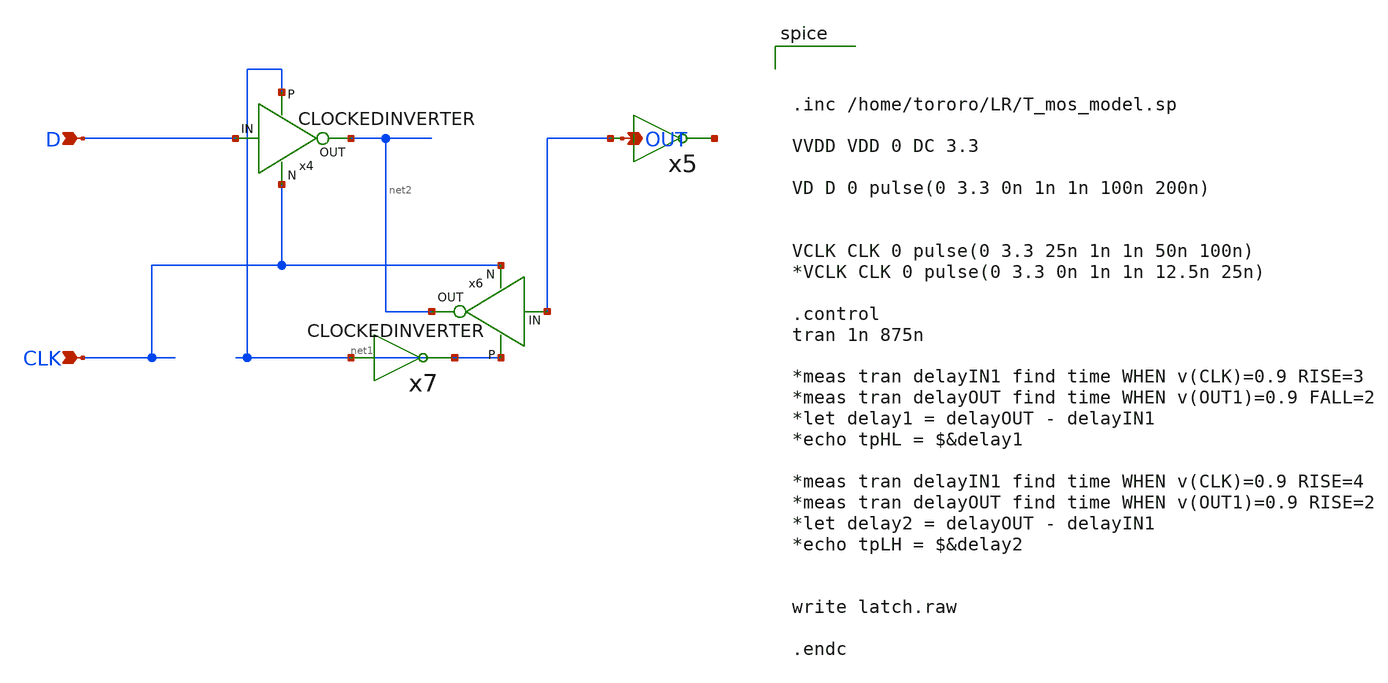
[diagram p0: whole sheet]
** sch_path: LR_hasegawa/LR_Work2/latch.sch
**.subckt latch D CLK OUT
*.ipin D
*.ipin CLK
*.opin OUT
x5 OUT net3 INVERTER
x7 net1 net1 INVERTER
x4 net1 net2 D CLK CLOCKEDINVERTER
x6 net1 net2 OUT CLK CLOCKEDINVERTER
**** begin user architecture code



.inc /home/tororo/LR/T_mos_model.sp

VVDD VDD 0 DC 3.3

VD D 0 pulse(0 3.3 0n 1n 1n 100n 200n)


VCLK CLK 0 pulse(0 3.3 25n 1n 1n 50n 100n)
*VCLK CLK 0 pulse(0 3.3 0n 1n 1n 12.5n 25n)

.control
tran 1n 875n

*meas tran delayIN1 find time WHEN v(CLK)=0.9 RISE=3
*meas tran delayOUT find time WHEN v(OUT1)=0.9 FALL=2
*let delay1 = delayOUT - delayIN1
*echo tpHL = $&delay1

*meas tran delayIN1 find time WHEN v(CLK)=0.9 RISE=4
*meas tran delayOUT find time WHEN v(OUT1)=0.9 RISE=2
*let delay2 = delayOUT - delayIN1
*echo tpLH = $&delay2


write latch.raw

.endc

**** end user architecture code
**.ends
.end
